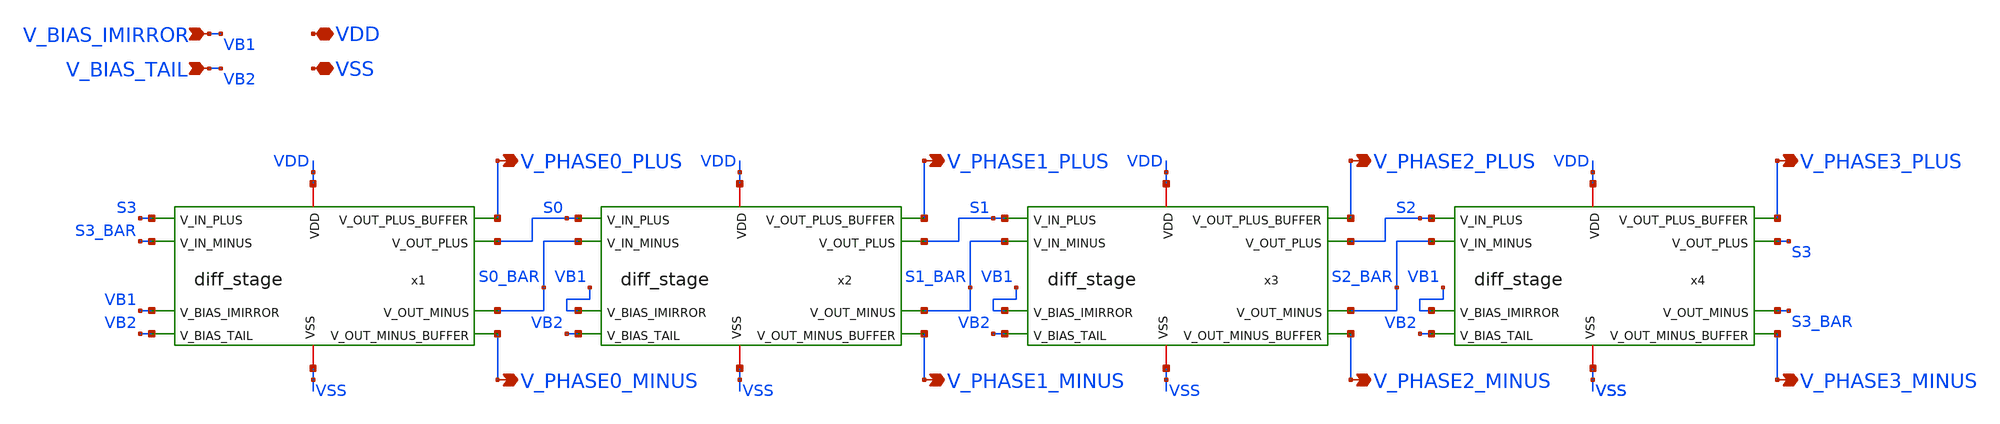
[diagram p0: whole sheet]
** sch_path: xschem/vco_core.sch
**.subckt vco_core V_PHASE0_PLUS V_PHASE1_PLUS V_PHASE2_PLUS V_PHASE3_PLUS V_PHASE0_MINUS
*+ V_PHASE1_MINUS V_PHASE2_MINUS V_PHASE3_MINUS V_BIAS_IMIRROR V_BIAS_TAIL VDD VSS
*.opin V_PHASE0_PLUS
*.opin V_PHASE1_PLUS
*.opin V_PHASE2_PLUS
*.opin V_PHASE3_PLUS
*.opin V_PHASE0_MINUS
*.opin V_PHASE1_MINUS
*.opin V_PHASE2_MINUS
*.opin V_PHASE3_MINUS
*.ipin V_BIAS_IMIRROR
*.ipin V_BIAS_TAIL
*.iopin VDD
*.iopin VSS
x1 VDD VSS S0_BAR S0 V_PHASE0_MINUS V_PHASE0_PLUS S3 S3_BAR VB1 VB2 diff_stage
x2 VDD VSS S1_BAR S1 V_PHASE1_MINUS V_PHASE1_PLUS S0 S0_BAR VB1 VB2 diff_stage
x3 VDD VSS S2_BAR S2 V_PHASE2_MINUS V_PHASE2_PLUS S1 S1_BAR VB1 VB2 diff_stage
x4 VDD VSS S3_BAR S3 V_PHASE3_MINUS V_PHASE3_PLUS S2 S2_BAR VB1 VB2 diff_stage
**.ends

* expanding   symbol:  diff_stage.sym # of pins=10
** sym_path: xschem/diff_stage.sym
** sch_path: xschem/diff_stage.sch
.subckt diff_stage VDD VSS V_OUT_MINUS V_OUT_PLUS V_OUT_MINUS_BUFFER V_OUT_PLUS_BUFFER V_IN_PLUS
+ V_IN_MINUS V_BIAS_IMIRROR V_BIAS_TAIL
*.opin V_OUT_PLUS
*.opin V_OUT_PLUS_BUFFER
*.opin V_OUT_MINUS
*.opin V_OUT_MINUS_BUFFER
*.ipin V_BIAS_IMIRROR
*.ipin V_IN_MINUS
*.ipin V_IN_PLUS
*.ipin V_BIAS_TAIL
*.iopin VDD
*.iopin VSS
x1 VDD V_OUT_MINUS V_BIAS_IMIRROR V_OUT_PLUS V_OUT_PLUS_BUFFER V_IN_MINUS VSS V_DRAIN_TAIL
+ diff_stage_half
x2 VDD V_OUT_PLUS V_BIAS_IMIRROR V_OUT_MINUS V_OUT_MINUS_BUFFER V_IN_PLUS VSS V_DRAIN_TAIL
+ diff_stage_half
XM1 V_DRAIN_TAIL V_BIAS_TAIL VSS VSS sky130_fd_pr__nfet_01v8 L=2 W=4 nf=2 ad='int((nf+1)/2) * W/nf * 0.29'
+ as='int((nf+2)/2) * W/nf * 0.29' pd='2*int((nf+1)/2) * (W/nf + 0.29)' ps='2*int((nf+2)/2) * (W/nf + 0.29)'
+ nrd='0.29 / W' nrs='0.29 / W' sa=0 sb=0 sd=0 mult=1 m=1
.ends


* expanding   symbol:  diff_stage_half.sym # of pins=8
** sym_path: xschem/diff_stage_half.sym
** sch_path: xschem/diff_stage_half.sch
.subckt diff_stage_half VDD V_FB_CROSSCOUPLED V_BIAS_IMIRROR V_OUT_DIFF V_OUT_DIFF_BUFFER V_IN_RING
+ VSS V_DRAIN_TAIL
*.ipin V_BIAS_IMIRROR
*.ipin V_FB_CROSSCOUPLED
*.ipin V_IN_RING
*.opin V_OUT_DIFF
*.iopin VDD
*.iopin VSS
*.opin V_OUT_DIFF_BUFFER
*.iopin V_DRAIN_TAIL
XM1 V_OUT_DIFF V_BIAS_IMIRROR VDD VDD sky130_fd_pr__pfet_01v8 L=2 W=4 nf=2 ad='int((nf+1)/2) * W/nf * 0.29'
+ as='int((nf+2)/2) * W/nf * 0.29' pd='2*int((nf+1)/2) * (W/nf + 0.29)' ps='2*int((nf+2)/2) * (W/nf + 0.29)'
+ nrd='0.29 / W' nrs='0.29 / W' sa=0 sb=0 sd=0 mult=1 m=1
XM2 V_OUT_DIFF V_FB_CROSSCOUPLED VDD VDD sky130_fd_pr__pfet_01v8 L=2 W=4 nf=2 ad='int((nf+1)/2) * W/nf * 0.29'
+ as='int((nf+2)/2) * W/nf * 0.29' pd='2*int((nf+1)/2) * (W/nf + 0.29)' ps='2*int((nf+2)/2) * (W/nf + 0.29)'
+ nrd='0.29 / W' nrs='0.29 / W' sa=0 sb=0 sd=0 mult=1 m=1
XM3 V_OUT_DIFF V_IN_RING V_DRAIN_TAIL VSS sky130_fd_pr__nfet_01v8 L=2 W=4 nf=2 ad='int((nf+1)/2) * W/nf * 0.29'
+ as='int((nf+2)/2) * W/nf * 0.29' pd='2*int((nf+1)/2) * (W/nf + 0.29)' ps='2*int((nf+2)/2) * (W/nf + 0.29)'
+ nrd='0.29 / W' nrs='0.29 / W' sa=0 sb=0 sd=0 mult=1 m=1
XM4 VSS V_OUT_DIFF VSS VSS sky130_fd_pr__nfet_01v8 L=11 W=11 nf=1 ad='int((nf+1)/2) * W/nf * 0.29' as='int((nf+2)/2) * W/nf * 0.29'
+ pd='2*int((nf+1)/2) * (W/nf + 0.29)' ps='2*int((nf+2)/2) * (W/nf + 0.29)' nrd='0.29 / W' nrs='0.29 / W'
+ sa=0 sb=0 sd=0 mult=1 m=1
x1 VDD VSS V_OUT_DIFF_BUFFER V_OUT_DIFF min_buffer
.ends


* expanding   symbol:  min_buffer.sym # of pins=4
** sym_path: xschem/min_buffer.sym
** sch_path: xschem/min_buffer.sch
.subckt min_buffer VDD VSS VOUT_BUFFER VIN_BUFFER
*.ipin VIN_BUFFER
*.opin VOUT_BUFFER
*.iopin VDD
*.iopin VSS
x1 VDD VSS VOUT_BUFFER INT_BUFFER min_inv
x2 VDD VSS INT_BUFFER VIN_BUFFER min_inv
.ends


* expanding   symbol:  min_inv.sym # of pins=4
** sym_path: xschem/min_inv.sym
** sch_path: xschem/min_inv.sch
.subckt min_inv VDD VSS VOUT_INV VIN_INV
*.iopin VDD
*.iopin VSS
*.ipin VIN_INV
*.opin VOUT_INV
XM2 VOUT_INV VIN_INV VSS VSS sky130_fd_pr__nfet_01v8 L=0.15 W=1 nf=1 ad='int((nf+1)/2) * W/nf * 0.29'
+ as='int((nf+2)/2) * W/nf * 0.29' pd='2*int((nf+1)/2) * (W/nf + 0.29)' ps='2*int((nf+2)/2) * (W/nf + 0.29)'
+ nrd='0.29 / W' nrs='0.29 / W' sa=0 sb=0 sd=0 mult=1 m=1
XM3 VOUT_INV VIN_INV VDD VDD sky130_fd_pr__pfet_01v8 L=0.15 W=1 nf=1 ad='int((nf+1)/2) * W/nf * 0.29'
+ as='int((nf+2)/2) * W/nf * 0.29' pd='2*int((nf+1)/2) * (W/nf + 0.29)' ps='2*int((nf+2)/2) * (W/nf + 0.29)'
+ nrd='0.29 / W' nrs='0.29 / W' sa=0 sb=0 sd=0 mult=1 m=1
.ends

.end
